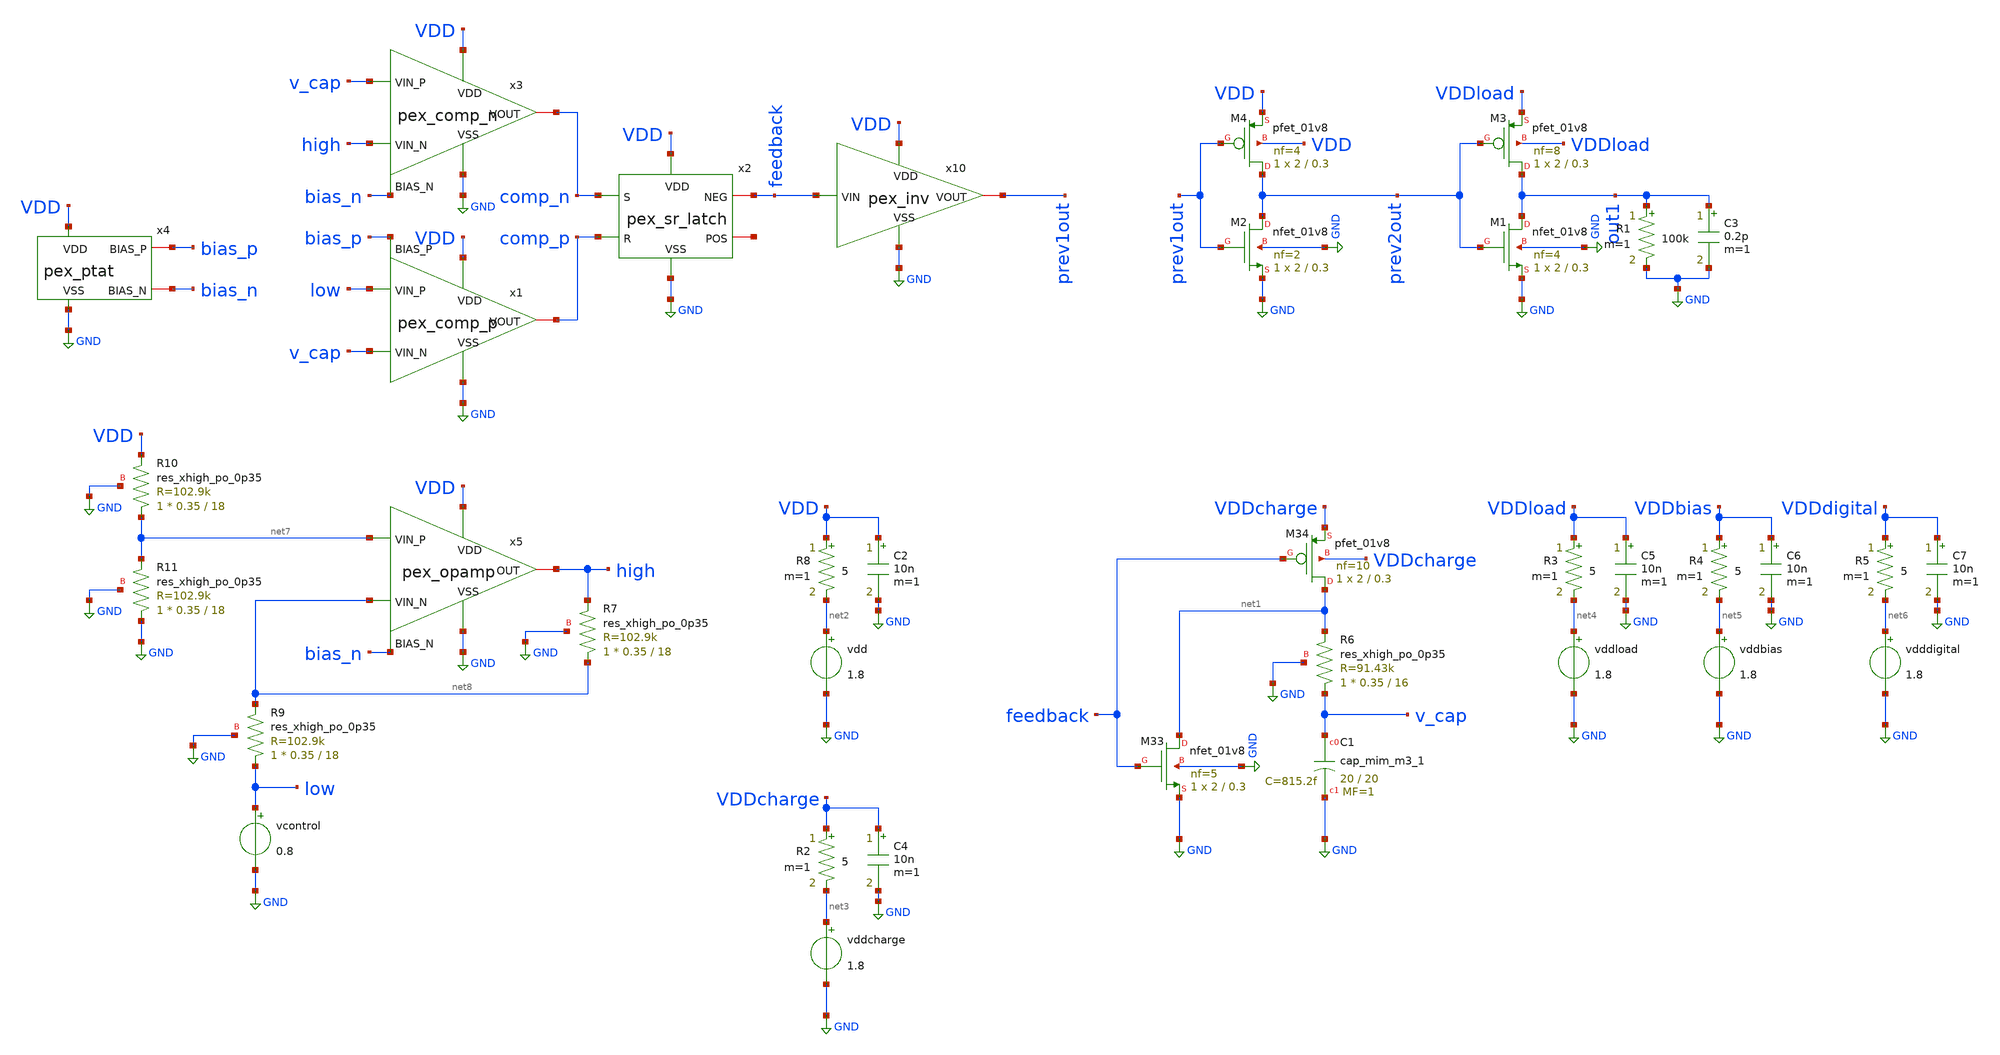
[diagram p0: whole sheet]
** sch_path: schem/tb/pex_full.sch
**.subckt pex_full
XC1 v_cap GND sky130_fd_pr__cap_mim_m3_1 W=20 L=20 MF=1 m=1
XM33 net1 feedback GND GND sky130_fd_pr__nfet_01v8 L=0.3 W=2 nf=5 ad='int((5 + 1)/2) * 2 / 5 * 0.29'
+ as='int((5 + 2)/2) * 2 / 5 * 0.29' pd='2*int((5 + 1)/2) * (2 / 5 + 0.29)' ps='2*int((5 + 2)/2) * (2 / 5 + 0.29)'
+ nrd='0.29 / 2 ' nrs='0.29 / 2 ' sa=0 sb=0 sd=0 mult=1 m=1
XM34 net1 feedback VDDcharge VDDcharge sky130_fd_pr__pfet_01v8 L=0.3 W=2 nf=10 ad='int((10 + 1)/2) * 2 / 10 * 0.29'
+ as='int((10 + 2)/2) * 2 / 10 * 0.29' pd='2*int((10 + 1)/2) * (2 / 10 + 0.29)' ps='2*int((10 + 2)/2) * (2 / 10 + 0.29)'
+ nrd='0.29 / 2 ' nrs='0.29 / 2 ' sa=0 sb=0 sd=0 mult=1 m=1
vdd net2 GND 1.8
C2 VDD GND 10n m=1
R8 VDD net2 5 m=1
vddcharge net3 GND 1.8
C4 VDDcharge GND 10n m=1
R2 VDDcharge net3 5 m=1
R1 out1 GND 100k m=1
C3 out1 GND 0.2p m=1
vddload net4 GND 1.8
C5 VDDload GND 10n m=1
R3 VDDload net4 5 m=1
vddbias net5 GND 1.8
C6 VDDbias GND 10n m=1
R4 VDDbias net5 5 m=1
vdddigital net6 GND 1.8
C7 VDDdigital GND 10n m=1
R5 VDDdigital net6 5 m=1
XM1 out1 prev2out GND GND sky130_fd_pr__nfet_01v8 L=0.3 W=2 nf=4 ad='int((4 + 1)/2) * 2 / 4 * 0.29' as='int((4 + 2)/2) * 2 / 4 * 0.29'
+ pd='2*int((4 + 1)/2) * (2 / 4 + 0.29)' ps='2*int((4 + 2)/2) * (2 / 4 + 0.29)' nrd='0.29 / 2 ' nrs='0.29 / 2 '
+ sa=0 sb=0 sd=0 mult=1 m=1
XM3 out1 prev2out VDDload VDDload sky130_fd_pr__pfet_01v8 L=0.3 W=2 nf=8 ad='int((8 + 1)/2) * 2 / 8 * 0.29'
+ as='int((8 + 2)/2) * 2 / 8 * 0.29' pd='2*int((8 + 1)/2) * (2 / 8 + 0.29)' ps='2*int((8 + 2)/2) * (2 / 8 + 0.29)'
+ nrd='0.29 / 2 ' nrs='0.29 / 2 ' sa=0 sb=0 sd=0 mult=1 m=1
XM2 prev2out prev1out GND GND sky130_fd_pr__nfet_01v8 L=0.3 W=2 nf=2 ad='int((2 + 1)/2) * 2 / 2 * 0.29'
+ as='int((2 + 2)/2) * 2 / 2 * 0.29' pd='2*int((2 + 1)/2) * (2 / 2 + 0.29)' ps='2*int((2 + 2)/2) * (2 / 2 + 0.29)'
+ nrd='0.29 / 2 ' nrs='0.29 / 2 ' sa=0 sb=0 sd=0 mult=1 m=1
XM4 prev2out prev1out VDD VDD sky130_fd_pr__pfet_01v8 L=0.3 W=2 nf=4 ad='int((4 + 1)/2) * 2 / 4 * 0.29'
+ as='int((4 + 2)/2) * 2 / 4 * 0.29' pd='2*int((4 + 1)/2) * (2 / 4 + 0.29)' ps='2*int((4 + 2)/2) * (2 / 4 + 0.29)'
+ nrd='0.29 / 2 ' nrs='0.29 / 2 ' sa=0 sb=0 sd=0 mult=1 m=1
vcontrol low GND 0.8
x5 VDD GND net7 net8 high bias_n opamp
x10 VDD feedback prev1out GND inv_1
x3 VDD GND high v_cap comp_n bias_n comp_n
x1 VDD GND bias_p comp_p low v_cap comp_p
x2 VDD GND comp_p comp_n feedback net9 sr_latch
x4 VDD GND bias_p bias_n ptat
XR6 v_cap net1 GND sky130_fd_pr__res_xhigh_po_0p35 L=16 mult=1 m=1
XR7 net8 high GND sky130_fd_pr__res_xhigh_po_0p35 L=18 mult=1 m=1
XR9 low net8 GND sky130_fd_pr__res_xhigh_po_0p35 L=18 mult=1 m=1
XR10 net7 VDD GND sky130_fd_pr__res_xhigh_po_0p35 L=18 mult=1 m=1
XR11 GND net7 GND sky130_fd_pr__res_xhigh_po_0p35 L=18 mult=1 m=1
**** begin user architecture code



.include /home/zhixuan/projects/fyp_vco/magic/ip/comp_p/comp_p.spice
.include /home/zhixuan/projects/fyp_vco/magic/ip/comp_n/comp_n.spice
.include /home/zhixuan/projects/fyp_vco/magic/ip/sr_latch/sr_latch.spice
.include /home/zhixuan/projects/fyp_vco/magic/ip/inv_1/inv_1.spice
.include /home/zhixuan/projects/fyp_vco/magic/ip/pseudo_res/pseudo_res.spice
.include /home/zhixuan/projects/fyp_vco/magic/ip/ptat/ptat.spice
.include /home/zhixuan/projects/fyp_vco/magic/ip/opamp/opamp.spice


.lib /usr/local/share/pdk/sky130A/libs.tech/ngspice/sky130.lib.spice tt

.tran 0.1n 2u
.save all

.control
    run

    * Find rising edges of feedback signal (threshold at 0.9V for 1.8V signal)
    meas tran t1 when feedback=0.9 rise=2
    meas tran t2 when feedback=0.9 rise=3

    * Calculate period and frequency from 2nd period onwards
    let period = t2 - t1
    let freq = 1 / period

    print period
    print freq

    plot low high v_cap prev1out out1
    plot abs(i(vdd))*1.8 + abs(i(vddcharge))*1.8
.endc

.end


**** end user architecture code
**.ends
.GLOBAL GND
.end
